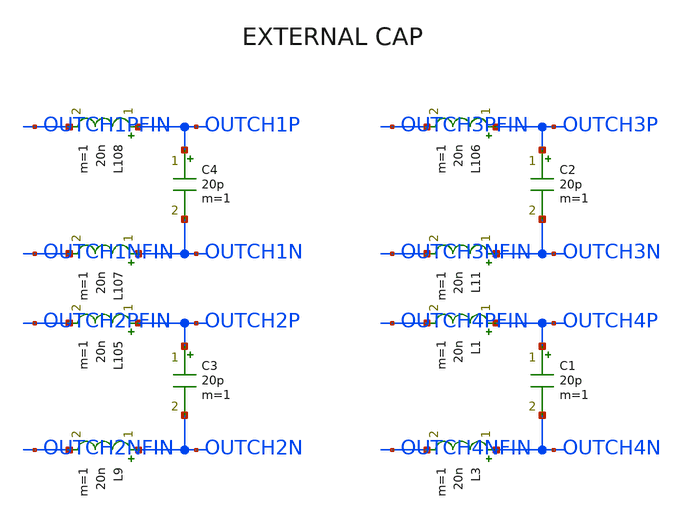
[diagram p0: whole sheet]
** sch_path: ISSCC26/submitted_notebooks/Low Mismatch 4 Channels Instrumentation Amplifier EEG/Top Integrations/Schematic/EXT_OPTIONAL_CAP.sch
**.subckt EXT_OPTIONAL_CAP
L1 OUTCH4P OUTCH4PFIN 20n m=1
L3 OUTCH4N OUTCH4NFIN 20n m=1
C1 OUTCH4P OUTCH4N 20p m=1
L9 OUTCH2N OUTCH2NFIN 20n m=1
L11 OUTCH3N OUTCH3NFIN 20n m=1
C2 OUTCH3P OUTCH3N 20p m=1
L105 OUTCH2P OUTCH2PFIN 20n m=1
C3 OUTCH2P OUTCH2N 20p m=1
L106 OUTCH3P OUTCH3PFIN 20n m=1
L107 OUTCH1N OUTCH1NFIN 20n m=1
L108 OUTCH1P OUTCH1PFIN 20n m=1
C4 OUTCH1P OUTCH1N 20p m=1
**.ends
.end
